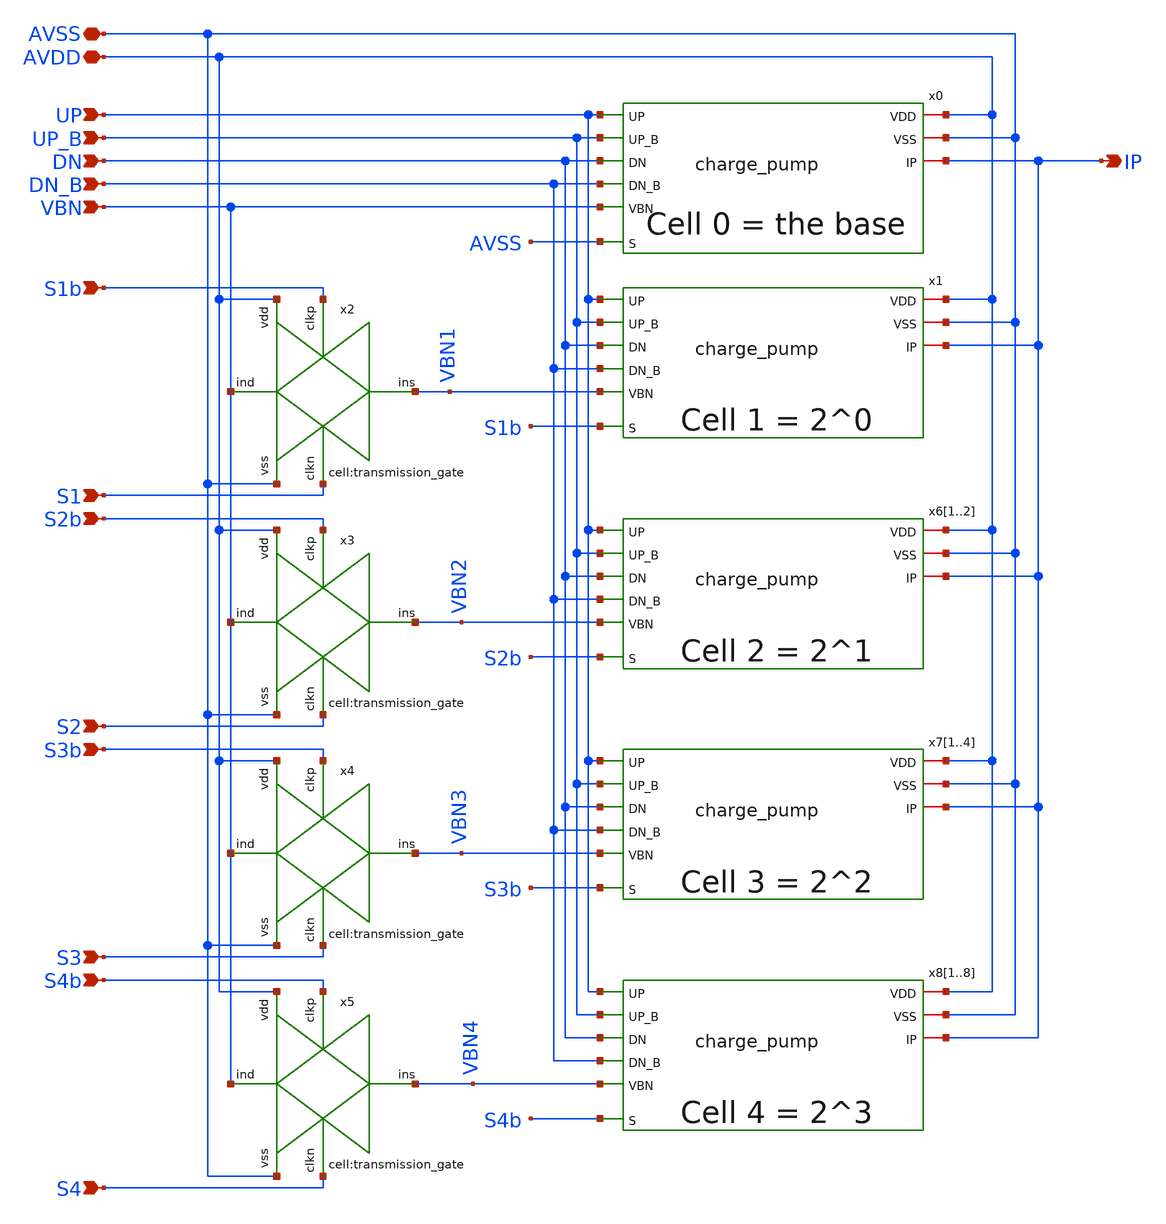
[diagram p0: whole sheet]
** sch_path: designs/libs/core_analog/programmable_charge_pump/programmable_charge_pump.sch
**.subckt programmable_charge_pump VBN S1b S1 S2b S2 S3b S3 S4b S4 AVSS AVDD UP UP_B DN DN_B IP
*.ipin VBN
*.ipin S1b
*.ipin S1
*.ipin S2b
*.ipin S2
*.ipin S3b
*.ipin S3
*.ipin S4b
*.ipin S4
*.iopin AVSS
*.iopin AVDD
*.ipin UP
*.ipin UP_B
*.ipin DN
*.ipin DN_B
*.opin IP
x1 AVDD AVSS UP UP_B DN DN_B VBN1 IP S1b charge_pump
x61 AVDD AVSS UP UP_B DN DN_B VBN2 IP S2b charge_pump
x62 AVDD AVSS UP UP_B DN DN_B VBN2 IP S2b charge_pump
x71 AVDD AVSS UP UP_B DN DN_B VBN3 IP S3b charge_pump
x72 AVDD AVSS UP UP_B DN DN_B VBN3 IP S3b charge_pump
x73 AVDD AVSS UP UP_B DN DN_B VBN3 IP S3b charge_pump
x74 AVDD AVSS UP UP_B DN DN_B VBN3 IP S3b charge_pump
x81 AVDD AVSS UP UP_B DN DN_B VBN4 IP S4b charge_pump
x82 AVDD AVSS UP UP_B DN DN_B VBN4 IP S4b charge_pump
x83 AVDD AVSS UP UP_B DN DN_B VBN4 IP S4b charge_pump
x84 AVDD AVSS UP UP_B DN DN_B VBN4 IP S4b charge_pump
x85 AVDD AVSS UP UP_B DN DN_B VBN4 IP S4b charge_pump
x86 AVDD AVSS UP UP_B DN DN_B VBN4 IP S4b charge_pump
x87 AVDD AVSS UP UP_B DN DN_B VBN4 IP S4b charge_pump
x88 AVDD AVSS UP UP_B DN DN_B VBN4 IP S4b charge_pump
x2 VBN AVSS S1 VBN1 S1b AVDD transmission_gate
x0 AVDD AVSS UP UP_B DN DN_B VBN IP AVSS charge_pump
x3 VBN AVSS S2 VBN2 S2b AVDD transmission_gate
x4 VBN AVSS S3 VBN3 S3b AVDD transmission_gate
x5 VBN AVSS S4 VBN4 S4b AVDD transmission_gate
**.ends

* expanding   symbol:  libs/core_analog/charge_pump/charge_pump.sym # of pins=9
** sym_path: designs/libs/core_analog/charge_pump/charge_pump.sym
** sch_path: designs/libs/core_analog/charge_pump/charge_pump.sch
.subckt charge_pump VDD VSS UP UP_B DN DN_B VBN IP S
*.iopin VDD
*.iopin VSS
*.ipin UP
*.ipin UP_B
*.ipin DN
*.ipin DN_B
*.ipin VBN
*.iopin IP
*.ipin S
x1 net5 net5 VDD net5 VDD cp_sym_load
x2 net3 net3 VDD net3 VDD cp_sym_load
x3 net4 net4 VDD net4 VDD cp_sym_load
x4 net5 net5 VDD IP VDD cp_sym_load
XM1 net1 VBN VSS VSS nfet_03v3 L=0.5u W=11.25u nf=1 ad='int((nf+1)/2) * W/nf * 0.18u' as='int((nf+2)/2) * W/nf * 0.18u'
+ pd='2*int((nf+1)/2) * (W/nf + 0.18u)' ps='2*int((nf+2)/2) * (W/nf + 0.18u)' nrd='0.18u / W' nrs='0.18u / W'
+ sa=0 sb=0 sd=0 m=1
XM3 net5 DN net1 VSS nfet_03v3 L=0.5u W=2.08u nf=1 ad='int((nf+1)/2) * W/nf * 0.18u' as='int((nf+2)/2) * W/nf * 0.18u'
+ pd='2*int((nf+1)/2) * (W/nf + 0.18u)' ps='2*int((nf+2)/2) * (W/nf + 0.18u)' nrd='0.18u / W' nrs='0.18u / W'
+ sa=0 sb=0 sd=0 m=1
XM7 VBN S VSS VSS nfet_03v3 L=0.5u W=1u nf=1 ad='int((nf+1)/2) * W/nf * 0.18u' as='int((nf+2)/2) * W/nf * 0.18u'
+ pd='2*int((nf+1)/2) * (W/nf + 0.18u)' ps='2*int((nf+2)/2) * (W/nf + 0.18u)' nrd='0.18u / W' nrs='0.18u / W'
+ sa=0 sb=0 sd=0 m=1
XM8 VBN S VSS VSS nfet_03v3 L=0.5u W=1u nf=1 ad='int((nf+1)/2) * W/nf * 0.18u' as='int((nf+2)/2) * W/nf * 0.18u'
+ pd='2*int((nf+1)/2) * (W/nf + 0.18u)' ps='2*int((nf+2)/2) * (W/nf + 0.18u)' nrd='0.18u / W' nrs='0.18u / W'
+ sa=0 sb=0 sd=0 m=1
XM4 net3 DN_B net1 VSS nfet_03v3 L=0.5u W=2.08u nf=1 ad='int((nf+1)/2) * W/nf * 0.18u' as='int((nf+2)/2) * W/nf * 0.18u'
+ pd='2*int((nf+1)/2) * (W/nf + 0.18u)' ps='2*int((nf+2)/2) * (W/nf + 0.18u)' nrd='0.18u / W' nrs='0.18u / W'
+ sa=0 sb=0 sd=0 m=1
XM5 net4 UP_B net2 VSS nfet_03v3 L=0.5u W=2.08u nf=1 ad='int((nf+1)/2) * W/nf * 0.18u' as='int((nf+2)/2) * W/nf * 0.18u'
+ pd='2*int((nf+1)/2) * (W/nf + 0.18u)' ps='2*int((nf+2)/2) * (W/nf + 0.18u)' nrd='0.18u / W' nrs='0.18u / W'
+ sa=0 sb=0 sd=0 m=1
XM6 IP UP net2 VSS nfet_03v3 L=0.5u W=2.08u nf=1 ad='int((nf+1)/2) * W/nf * 0.18u' as='int((nf+2)/2) * W/nf * 0.18u'
+ pd='2*int((nf+1)/2) * (W/nf + 0.18u)' ps='2*int((nf+2)/2) * (W/nf + 0.18u)' nrd='0.18u / W' nrs='0.18u / W'
+ sa=0 sb=0 sd=0 m=1
XM2 net2 VBN VSS VSS nfet_03v3 L=0.5u W=11.25u nf=1 ad='int((nf+1)/2) * W/nf * 0.18u' as='int((nf+2)/2) * W/nf * 0.18u'
+ pd='2*int((nf+1)/2) * (W/nf + 0.18u)' ps='2*int((nf+2)/2) * (W/nf + 0.18u)' nrd='0.18u / W' nrs='0.18u / W'
+ sa=0 sb=0 sd=0 m=1
.ends


* expanding   symbol:  libs/core_analog/transmission_gate/transmission_gate.sym # of pins=6
** sym_path: designs/libs/core_analog/transmission_gate/transmission_gate.sym
** sch_path: designs/libs/core_analog/transmission_gate/transmission_gate.sch
.subckt transmission_gate ind vss clkn ins clkp vdd
*.iopin ind
*.iopin ins
*.iopin clkn
*.iopin clkp
*.iopin vdd
*.iopin vss
XM1 ind clkp ins vdd pfet_03v3 L=0.5u W=3.0u nf=1 ad='int((nf+1)/2) * W/nf * 0.18u' as='int((nf+2)/2) * W/nf * 0.18u'
+ pd='2*int((nf+1)/2) * (W/nf + 0.18u)' ps='2*int((nf+2)/2) * (W/nf + 0.18u)' nrd='0.18u / W' nrs='0.18u / W'
+ sa=0 sb=0 sd=0 m=1
XM2 ind clkn ins vss nfet_03v3 L=0.5u W=1.0u nf=1 ad='int((nf+1)/2) * W/nf * 0.18u' as='int((nf+2)/2) * W/nf * 0.18u'
+ pd='2*int((nf+1)/2) * (W/nf + 0.18u)' ps='2*int((nf+2)/2) * (W/nf + 0.18u)' nrd='0.18u / W' nrs='0.18u / W'
+ sa=0 sb=0 sd=0 m=1
.ends


* expanding   symbol:  libs/core_analog/cp_sym_load/cp_sym_load.sym # of pins=5
** sym_path: designs/libs/core_analog/cp_sym_load/cp_sym_load.sym
** sch_path: designs/libs/core_analog/cp_sym_load/cp_sym_load.sch
.subckt cp_sym_load G1 G2 S D VDD
*.ipin G1
*.ipin G2
*.iopin S
*.iopin D
*.iopin VDD
XM1 D G1 S VDD pfet_03v3 L=1.5u W=1.1u nf=1 ad='int((nf+1)/2) * W/nf * 0.18u' as='int((nf+2)/2) * W/nf * 0.18u'
+ pd='2*int((nf+1)/2) * (W/nf + 0.18u)' ps='2*int((nf+2)/2) * (W/nf + 0.18u)' nrd='0.18u / W' nrs='0.18u / W'
+ sa=0 sb=0 sd=0 m=1
XM2 D G2 S VDD pfet_03v3 L=1.5u W=1.1u nf=1 ad='int((nf+1)/2) * W/nf * 0.18u' as='int((nf+2)/2) * W/nf * 0.18u'
+ pd='2*int((nf+1)/2) * (W/nf + 0.18u)' ps='2*int((nf+2)/2) * (W/nf + 0.18u)' nrd='0.18u / W' nrs='0.18u / W'
+ sa=0 sb=0 sd=0 m=1
.ends

.end
